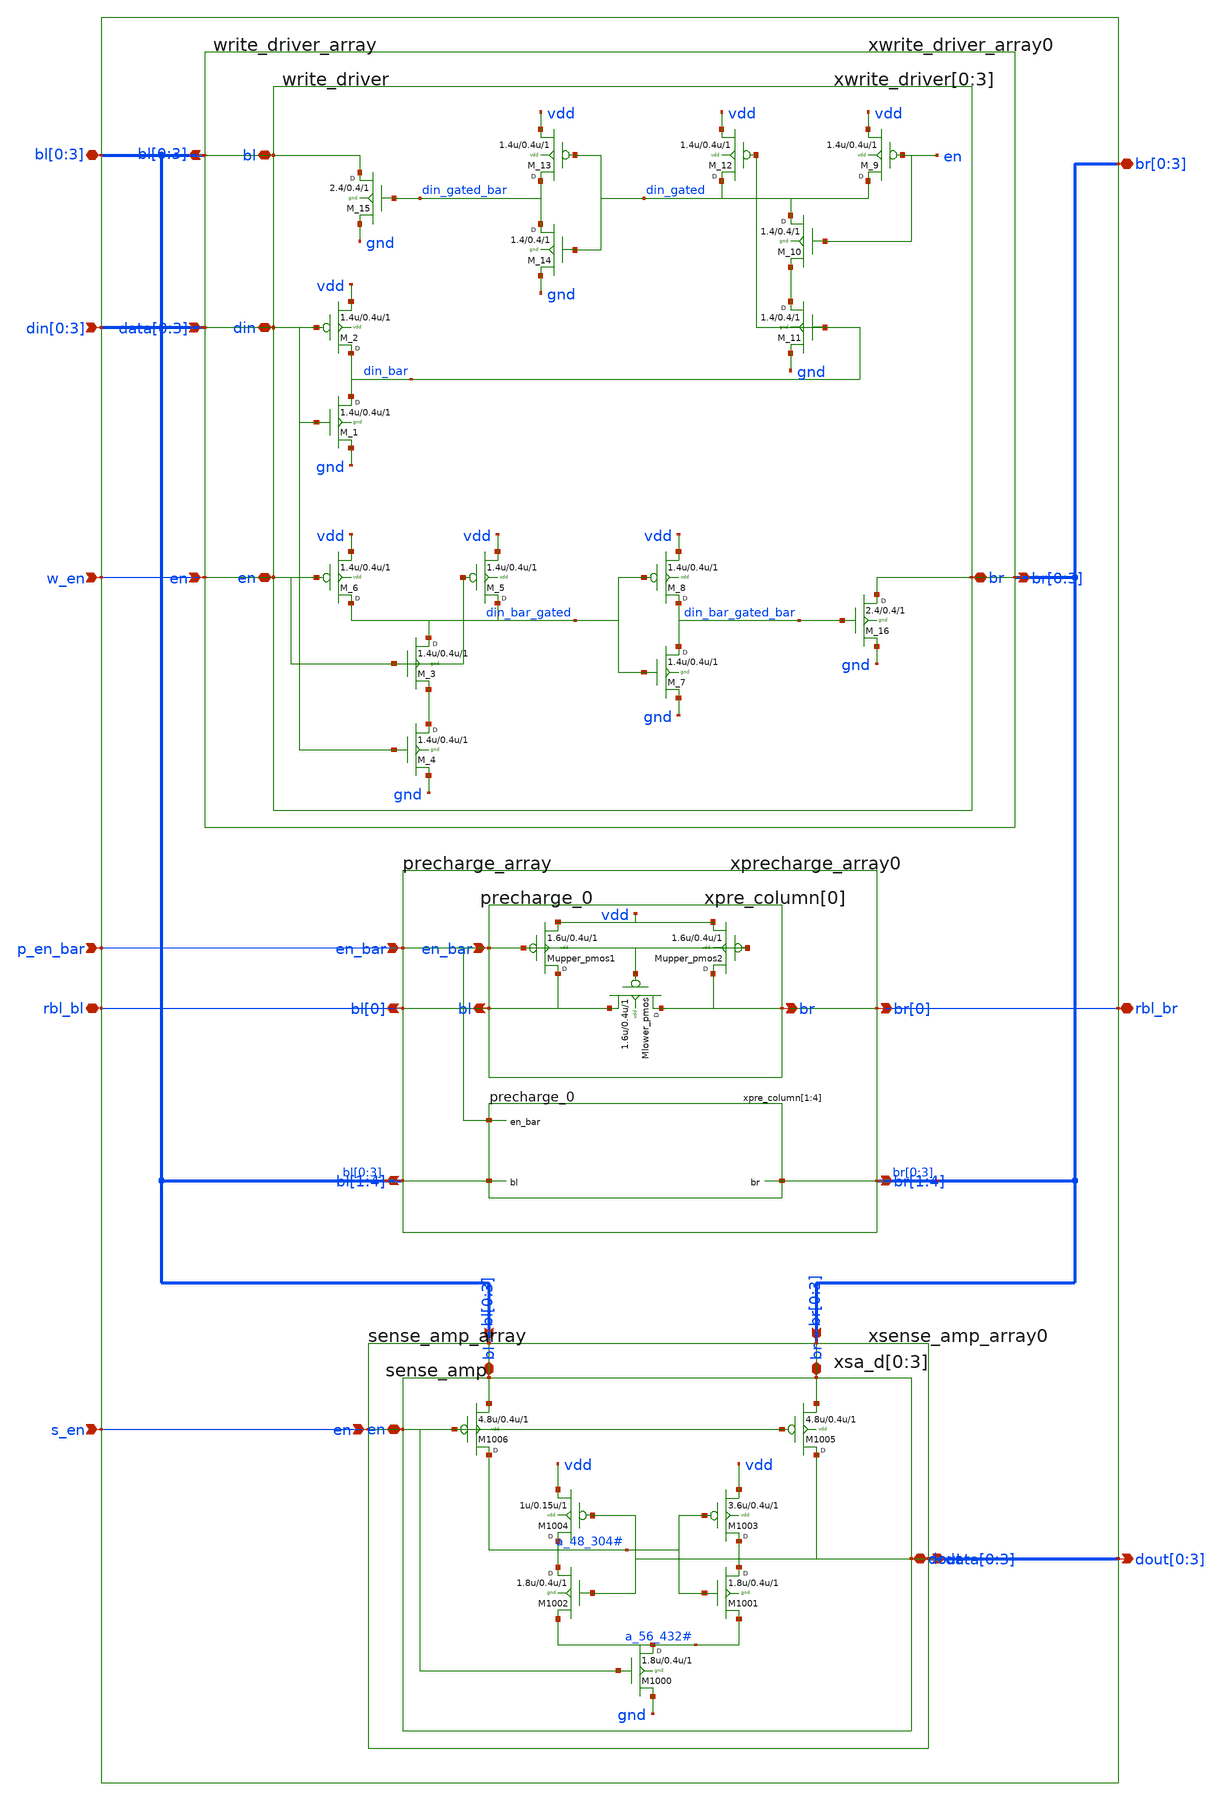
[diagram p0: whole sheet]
** sch_path: sram_4_16_scn4m/port_data.sch
**.subckt port_data rbl_bl rbl_br bl[0],bl[1],bl[2],bl[3] br[0],br[1],br[2],br[3]
*+ dout[0],dout[1],dout[2],dout[3] din[0],din[1],din[2],din[3] s_en p_en_bar w_en
*.iopin rbl_bl
*.iopin rbl_br
*.iopin bl[0],bl[1],bl[2],bl[3]
*.iopin br[0],br[1],br[2],br[3]
*.opin dout[0],dout[1],dout[2],dout[3]
*.ipin din[0],din[1],din[2],din[3]
*.ipin s_en
*.ipin p_en_bar
*.ipin w_en
xprecharge_array0 rbl_bl bl[0] bl[1] bl[2] bl[3] rbl_br br[0] br[1] br[2] br[3] p_en_bar vdd
+ precharge_array
xwrite_driver_array0 din[0] din[1] din[2] din[3] bl[0] bl[1] bl[2] bl[3] br[0] br[1] br[2] br[3]
+ w_en vdd gnd write_driver_array
xsense_amp_array0 dout[0] dout[1] dout[2] dout[3] bl[0] bl[1] bl[2] bl[3] br[0] br[1] br[2] br[3]
+ s_en vdd gnd sense_amp_array
**.ends

* expanding   symbol:  precharge_array.sch # of pins=5
** sym_path: sram_4_16_scn4m/precharge_array.sch
** sch_path: sram_4_16_scn4m/precharge_array.sch
.subckt precharge_array bl[0] bl[1] bl[2] bl[3] bl[4] br[0] br[1] br[2] br[3] br[4] en_bar vdd
*.opin bl[0]
*.opin br[0]
*.ipin en_bar
*.opin bl[1],bl[2],bl[3],bl[4]
*.opin br[1],br[2],br[3],br[4]
xpre_column[0] bl[0] br[0] en_bar vdd precharge_0
xpre_column[1] bl[1] br[1] en_bar vdd precharge_0
xpre_column[2] bl[2] br[2] en_bar vdd precharge_0
xpre_column[3] bl[3] br[3] en_bar vdd precharge_0
xpre_column[4] bl[4] br[4] en_bar vdd precharge_0
.ends


* expanding   symbol:  write_driver_array.sch # of pins=4
** sym_path: sram_4_16_scn4m/write_driver_array.sch
** sch_path: sram_4_16_scn4m/write_driver_array.sch
.subckt write_driver_array data[0] data[1] data[2] data[3] bl[0] bl[1] bl[2] bl[3] br[0] br[1] br[2]
+ br[3] en vdd gnd
*.ipin data[0],data[1],data[2],data[3]
*.opin bl[0],bl[1],bl[2],bl[3]
*.opin br[0],br[1],br[2],br[3]
*.ipin en
xwrite_driver[0] data[0] bl[0] br[0] en vdd gnd write_driver
xwrite_driver[1] data[1] bl[1] br[1] en vdd gnd write_driver
xwrite_driver[2] data[2] bl[2] br[2] en vdd gnd write_driver
xwrite_driver[3] data[3] bl[3] br[3] en vdd gnd write_driver
.ends


* expanding   symbol:  sense_amp_array.sch # of pins=4
** sym_path: sram_4_16_scn4m/sense_amp_array.sch
** sch_path: sram_4_16_scn4m/sense_amp_array.sch
.subckt sense_amp_array data[0] data[1] data[2] data[3] bl[0] bl[1] bl[2] bl[3] br[0] br[1] br[2]
+ br[3] en vdd gnd
*.opin data[0],data[1],data[2],data[3]
*.ipin bl[0],bl[1],bl[2],bl[3]
*.ipin br[0],br[1],br[2],br[3]
*.ipin en
xsa_d[0] bl[0] br[0] data[0] en vdd gnd sense_amp
xsa_d[1] bl[1] br[1] data[1] en vdd gnd sense_amp
xsa_d[2] bl[2] br[2] data[2] en vdd gnd sense_amp
xsa_d[3] bl[3] br[3] data[3] en vdd gnd sense_amp
.ends


* expanding   symbol:  precharge_0.sch # of pins=3
** sym_path: sram_4_16_scn4m/precharge_0.sch
** sch_path: sram_4_16_scn4m/precharge_0.sch
.subckt precharge_0 bl br en_bar vdd
*.opin bl
*.opin br
*.ipin en_bar
Mupper_pmos1 bl en_bar vdd vdd p w=1.6u l=0.4u m=1
Mupper_pmos2 br en_bar vdd vdd p w=1.6u l=0.4u m=1
Mlower_pmos br en_bar bl vdd p w=1.6u l=0.4u m=1
.ends


* expanding   symbol:  write_driver.sch # of pins=4
** sym_path: sram_4_16_scn4m/write_driver.sch
** sch_path: sram_4_16_scn4m/write_driver.sch
.subckt write_driver din bl br en vdd gnd
*.iopin din
*.iopin bl
*.iopin br
*.iopin en
M_1 din_bar din gnd gnd n w=1.4u l=0.4u m=1
M_2 din_bar din vdd vdd p w=1.4u l=0.4u m=1
M_6 din_bar_gated en vdd vdd p w=1.4u l=0.4u m=1
M_5 din_bar_gated en vdd vdd p w=1.4u l=0.4u m=1
M_3 din_bar_gated en net1 gnd n w=1.4u l=0.4u m=1
M_4 net1 din gnd gnd n w=1.4u l=0.4u m=1
M_7 din_bar_gated_bar din_bar_gated gnd gnd n w=1.4u l=0.4u m=1
M_8 din_bar_gated_bar din_bar_gated vdd vdd p w=1.4u l=0.4u m=1
M_9 din_gated en vdd vdd p w=1.4u l=0.4u m=1
M_12 din_gated din_bar vdd vdd p w=1.4u l=0.4u m=1
M_10 din_gated en net2 gnd n w=1.4 l=0.4 m=1
M_11 net2 din_bar gnd gnd n w=1.4 l=0.4 m=1
M_14 din_gated_bar din_gated gnd gnd n w=1.4 l=0.4 m=1
M_13 din_gated_bar din_gated vdd vdd p w=1.4u l=0.4u m=1
M_15 bl din_gated_bar gnd gnd n w=2.4 l=0.4 m=1
M_16 br din_bar_gated_bar gnd gnd n w=2.4 l=0.4 m=1
.ends


* expanding   symbol:  sense_amp.sch # of pins=4
** sym_path: sram_4_16_scn4m/sense_amp.sch
** sch_path: sram_4_16_scn4m/sense_amp.sch
.subckt sense_amp bl br dout en vdd gnd
*.iopin bl
*.iopin br
*.iopin dout
*.iopin en
M1004 a_48_304# dout vdd vdd p w=1u l=0.15u m=1
M1003 dout a_48_304# vdd vdd p w=3.6u l=0.4u m=1
M1002 a_48_304# dout a_56_432# gnd n w=1.8u l=0.4u m=1
M1001 dout a_48_304# a_56_432# gnd n w=1.8u l=0.4u m=1
M1000 a_56_432# en gnd gnd n w=1.8u l=0.4u m=1
M1006 a_48_304# en bl vdd p w=4.8u l=0.4u m=1
M1005 dout en br vdd p w=4.8u l=0.4u m=1
.ends

.end
